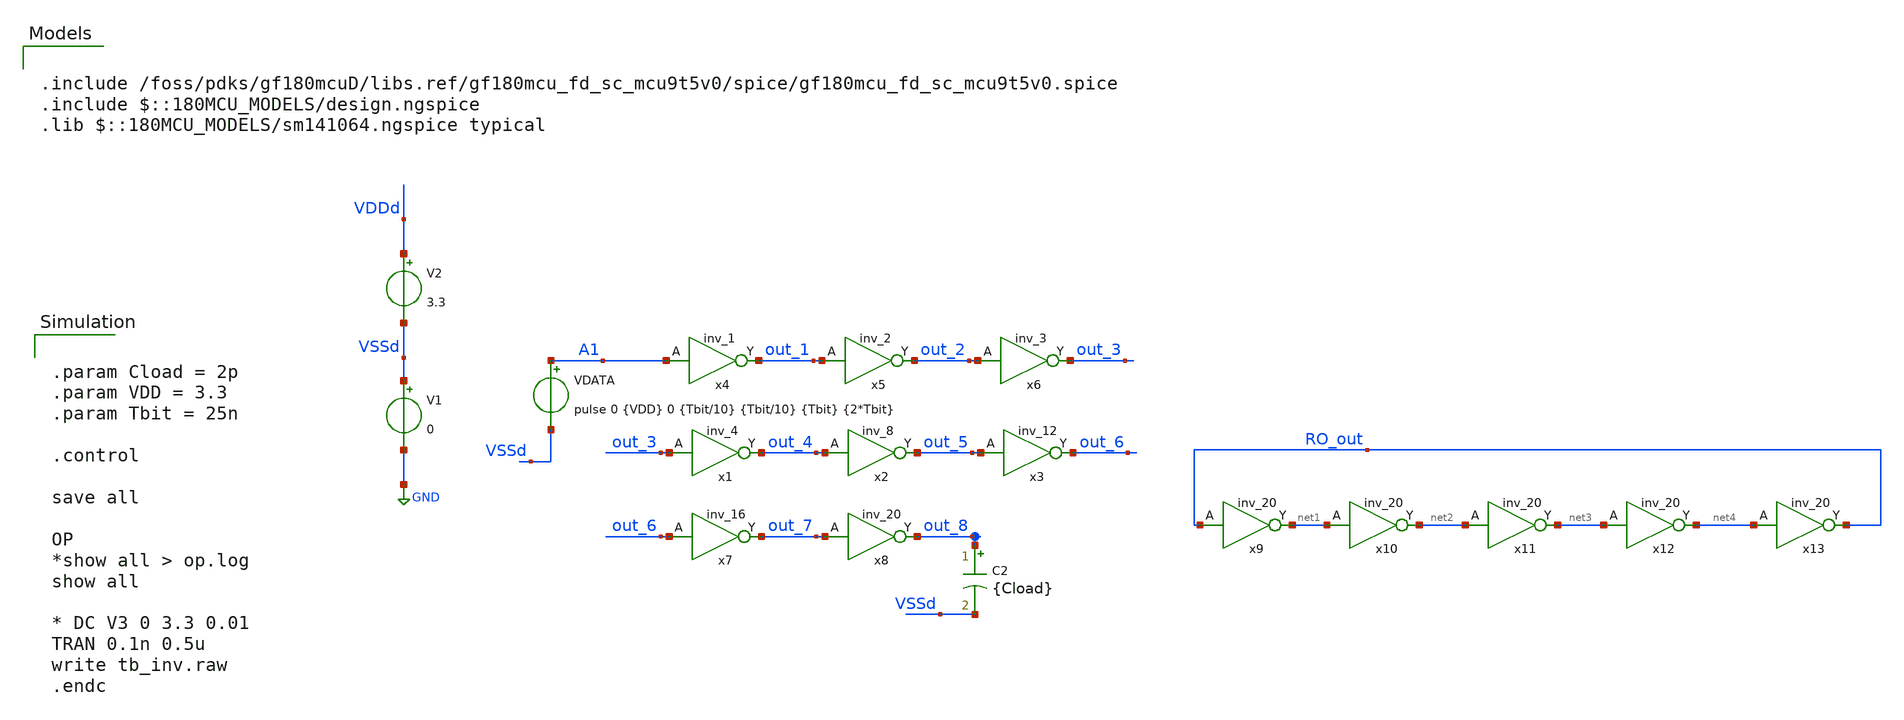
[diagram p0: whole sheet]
** sch_path: xschem/large_delay/tb_inv.sch
**.subckt tb_inv
V1 VSSd GND 0
V2 VDDd VSSd 3.3
VDATA A1 VSSd pulse 0 {VDD} 0 {Tbit/10} {Tbit/10} {Tbit} {2*Tbit}
x4 A1 VSSd VDDd VSSd VDDd out_1 gf180mcu_fd_sc_mcu9t5v0__inv_1
x5 out_1 VSSd VDDd VSSd VDDd out_2 gf180mcu_fd_sc_mcu9t5v0__inv_2
x6 out_2 out_3 VDDd VDDd VSSd VSSd gf180mcu_fd_sc_mcu9t5v0__inv_3
x1 out_3 VSSd VDDd VSSd VDDd out_4 gf180mcu_fd_sc_mcu9t5v0__inv_4
x2 out_4 VSSd VDDd VSSd VDDd out_5 gf180mcu_fd_sc_mcu9t5v0__inv_8
x3 out_5 VSSd VDDd VSSd VDDd out_6 gf180mcu_fd_sc_mcu9t5v0__inv_12
C2 out_8 VSSd {Cload} m=1
x8 out_7 out_8 VDDd VDDd VSSd VSSd gf180mcu_fd_sc_mcu9t5v0__inv_20
x7 out_6 VSSd VDDd VSSd VDDd out_7 gf180mcu_fd_sc_mcu9t5v0__inv_16
x9 RO_out net1 VDDd VDDd VSSd VSSd gf180mcu_fd_sc_mcu9t5v0__inv_20
x10 net1 net2 VDDd VDDd VSSd VSSd gf180mcu_fd_sc_mcu9t5v0__inv_20
x11 net2 net3 VDDd VDDd VSSd VSSd gf180mcu_fd_sc_mcu9t5v0__inv_20
x12 net3 net4 VDDd VDDd VSSd VSSd gf180mcu_fd_sc_mcu9t5v0__inv_20
x13 net4 RO_out VDDd VDDd VSSd VSSd gf180mcu_fd_sc_mcu9t5v0__inv_20
**** begin user architecture code


.param Cload = 2p
.param VDD = 3.3
.param Tbit = 25n

.control

save all

OP
*show all > op.log
show all

* DC V3 0 3.3 0.01
TRAN 0.1n 0.5u
write tb_inv.raw
.endc



.include /foss/pdks/gf180mcuD/libs.ref/gf180mcu_fd_sc_mcu9t5v0/spice/gf180mcu_fd_sc_mcu9t5v0.spice
.include $::180MCU_MODELS/design.ngspice
.lib $::180MCU_MODELS/sm141064.ngspice typical

**** end user architecture code
**.ends
.GLOBAL GND
.end
